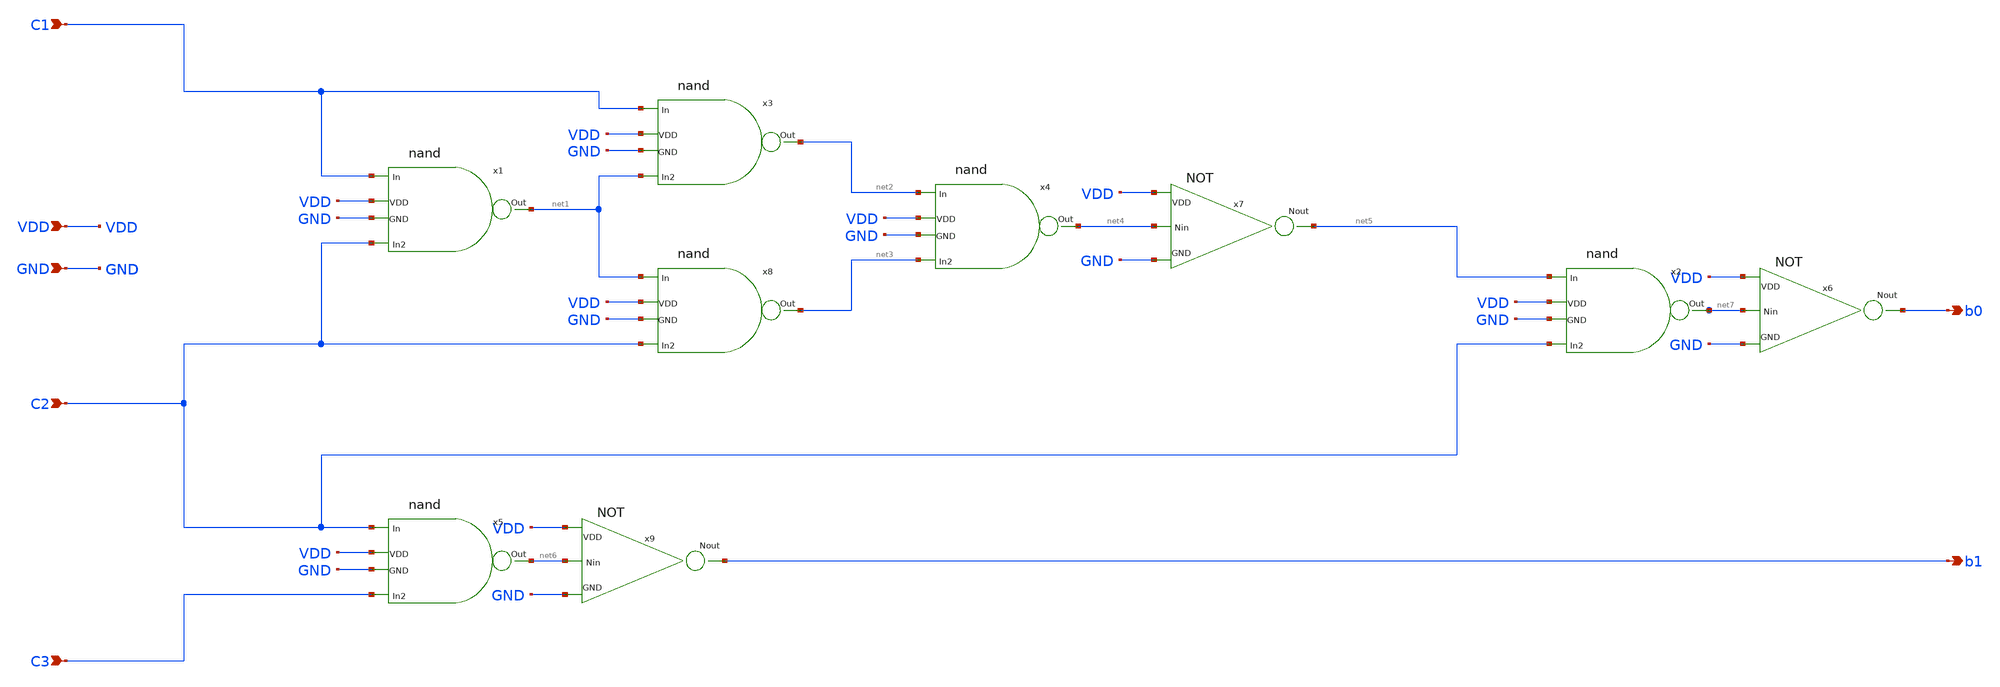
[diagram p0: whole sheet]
** sch_path: Analog Design Alan Rivera/Xschem/Sch/2BITENCODER.sch
**.subckt 2BITENCODER C1 C2 C3 b0 b1 VDD GND
*.ipin C1
*.ipin C2
*.ipin C3
*.opin b0
*.opin b1
*.ipin VDD
*.ipin GND
x9 VDD net6 b1 GND NOT
x5 VDD C2 C3 net6 GND nand
x2 VDD net5 C2 net7 GND nand
x6 VDD net7 b0 GND NOT
x7 VDD net4 net5 GND NOT
x4 VDD net2 net3 net4 GND nand
x3 VDD C1 net1 net2 GND nand
x8 VDD net1 C2 net3 GND nand
x1 VDD C1 C2 net1 GND nand
**.ends
.end
